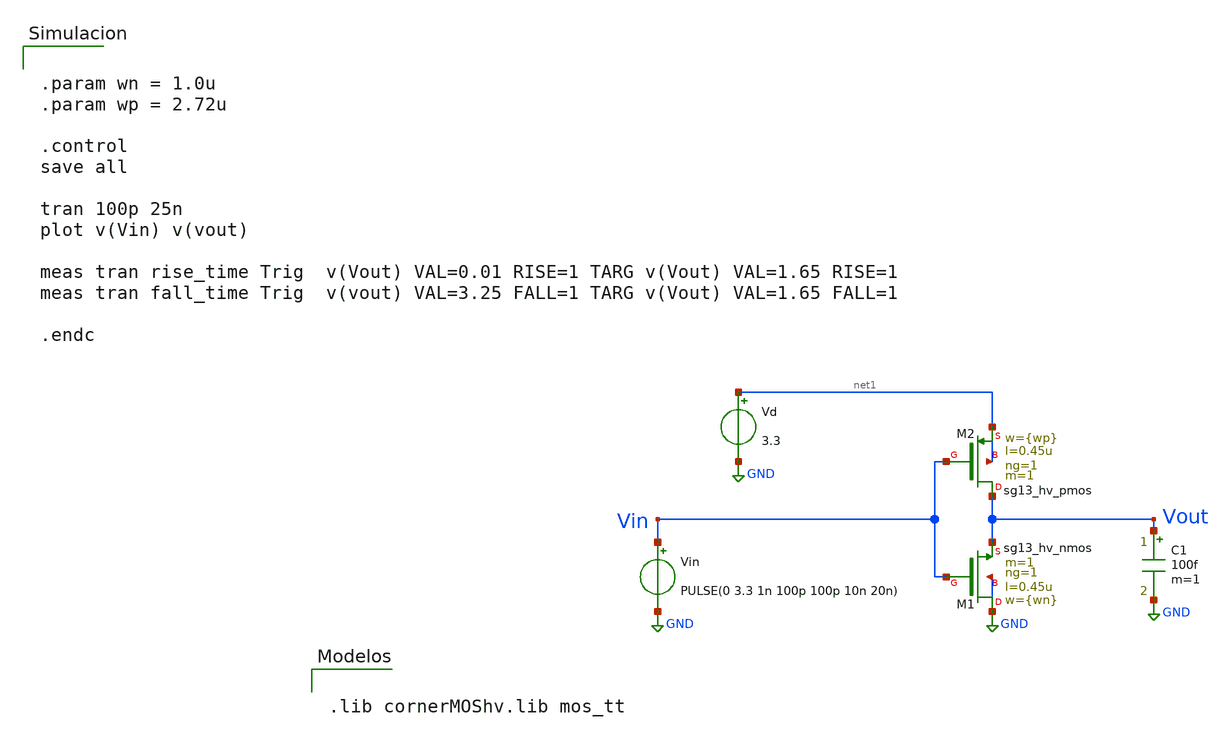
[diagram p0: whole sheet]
** sch_path: Taller2/Insumos/inv_hv_dimensionado.sch
**.subckt inv_hv_dimensionado
Vin Vin GND PULSE(0 3.3 1n 100p 100p 10n 20n)
Vd net1 GND 3.3
C1 Vout GND 100f m=1
XM1 GND Vin Vout GND sg13_hv_nmos w={wn} l=0.45u ng=1 m=1 mm_ok=1
XM2 Vout Vin net1 net1 sg13_hv_pmos w={wp} l=0.45u ng=1 m=1 mm_ok=1
**** begin user architecture code


.lib cornerMOShv.lib mos_tt




.param wn = 1.0u
.param wp = 2.72u

.control
save all

tran 100p 25n
plot v(Vin) v(vout)

meas tran rise_time Trig  v(Vout) VAL=0.01 RISE=1 TARG v(Vout) VAL=1.65 RISE=1
meas tran fall_time Trig  v(vout) VAL=3.25 FALL=1 TARG v(Vout) VAL=1.65 FALL=1

.endc


**** end user architecture code
**.ends
.GLOBAL GND
.end
